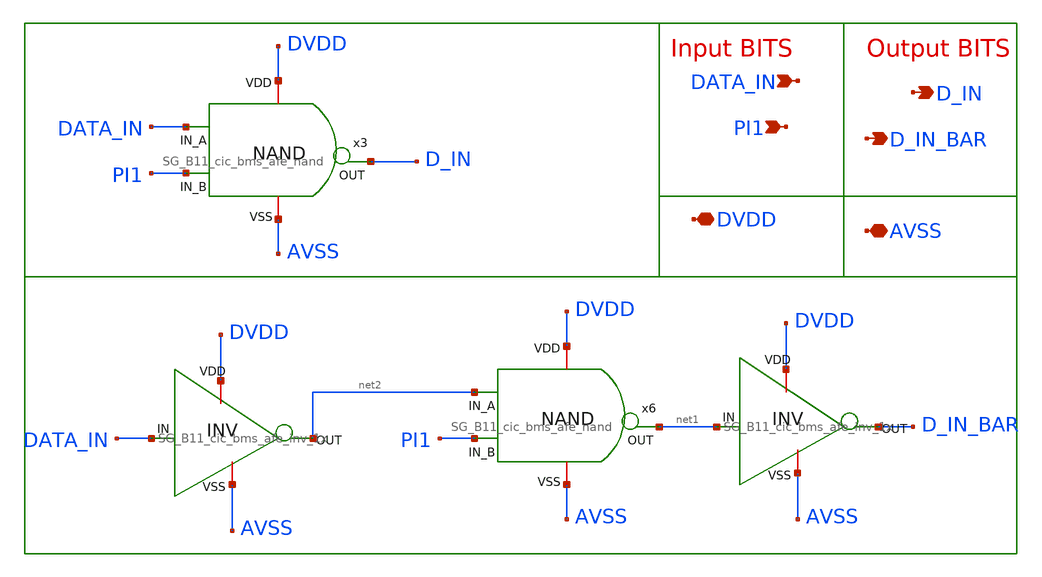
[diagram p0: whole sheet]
** sch_path: design/schematics/EIS/pkr_eis_control_logic.sch
**.subckt pkr_eis_control_logic DATA_IN PI1 DVDD AVSS D_IN D_IN_BAR
*.ipin DATA_IN
*.ipin PI1
*.iopin DVDD
*.iopin AVSS
*.opin D_IN
*.opin D_IN_BAR
x3 DVDD PI1 DATA_IN D_IN AVSS SG_B11_cic_bms_afe_nand
x5 DVDD D_IN_BAR net1 AVSS SG_B11_cic_bms_afe_inv_1x
x6 DVDD PI1 net2 net1 AVSS SG_B11_cic_bms_afe_nand
x4 DVDD net2 DATA_IN AVSS SG_B11_cic_bms_afe_inv_1x
**.ends

* expanding   symbol:  saakshath_designs/Non-overlapping _clk/SG_B11_cic_bms_afe_nand.sym # of
*+ pins=5
** sym_path: design/schematics/NOCG/SG_B11_cic_bms_afe_nand.sym
** sch_path: design/schematics/NOCG/SG_B11_cic_bms_afe_nand.sch
.subckt SG_B11_cic_bms_afe_nand VDD IN_B IN_A OUT VSS
*.iopin VDD
*.ipin IN_A
*.ipin IN_B
*.opin OUT
*.iopin VSS
XM1 OUT IN_A net1 VSS nfet_05v0 L=0.70u W=1.4u nf=1 ad='int((nf+1)/2) * W/nf * 0.18u' as='int((nf+2)/2) * W/nf * 0.18u'
+ pd='2*int((nf+1)/2) * (W/nf + 0.18u)' ps='2*int((nf+2)/2) * (W/nf + 0.18u)' nrd='0.18u / W' nrs='0.18u / W'
+ sa=0 sb=0 sd=0 m=1
XM2 net1 IN_B VSS VSS nfet_05v0 L=0.70u W=1.4u nf=1 ad='int((nf+1)/2) * W/nf * 0.18u' as='int((nf+2)/2) * W/nf * 0.18u'
+ pd='2*int((nf+1)/2) * (W/nf + 0.18u)' ps='2*int((nf+2)/2) * (W/nf + 0.18u)' nrd='0.18u / W' nrs='0.18u / W'
+ sa=0 sb=0 sd=0 m=1
XM3 OUT IN_B VDD VDD pfet_05v0 L=0.70u W=5.6u nf=1 ad='int((nf+1)/2) * W/nf * 0.18u' as='int((nf+2)/2) * W/nf * 0.18u'
+ pd='2*int((nf+1)/2) * (W/nf + 0.18u)' ps='2*int((nf+2)/2) * (W/nf + 0.18u)' nrd='0.18u / W' nrs='0.18u / W'
+ sa=0 sb=0 sd=0 m=1
XM4 OUT IN_A VDD VDD pfet_05v0 L=0.70u W=5.6u nf=1 ad='int((nf+1)/2) * W/nf * 0.18u' as='int((nf+2)/2) * W/nf * 0.18u'
+ pd='2*int((nf+1)/2) * (W/nf + 0.18u)' ps='2*int((nf+2)/2) * (W/nf + 0.18u)' nrd='0.18u / W' nrs='0.18u / W'
+ sa=0 sb=0 sd=0 m=1
.ends


* expanding   symbol:  saakshath_designs/Non-overlapping _clk/SG_B11_cic_bms_afe_inv_1x.sym # of
*+ pins=4
** sym_path: design/schematics/ADC/Non_Overlapping_clk_gen/SG_B11_cic_bms_afe_inv_1x.sym
** sch_path: design/schematics/ADC/Non_Overlapping_clk_gen/SG_B11_cic_bms_afe_inv_1x.sch
.subckt SG_B11_cic_bms_afe_inv_1x VDD OUT IN VSS
*.opin OUT
*.iopin VSS
*.iopin VDD
*.ipin IN
XM1 OUT IN VSS VSS nfet_05v0 L=0.70u W=1.4u nf=1 ad='int((nf+1)/2) * W/nf * 0.18u' as='int((nf+2)/2) * W/nf * 0.18u'
+ pd='2*int((nf+1)/2) * (W/nf + 0.18u)' ps='2*int((nf+2)/2) * (W/nf + 0.18u)' nrd='0.18u / W' nrs='0.18u / W'
+ sa=0 sb=0 sd=0 m=1
XM2 OUT IN VDD VDD pfet_05v0 L=0.70u W=5.6u nf=1 ad='int((nf+1)/2) * W/nf * 0.18u' as='int((nf+2)/2) * W/nf * 0.18u'
+ pd='2*int((nf+1)/2) * (W/nf + 0.18u)' ps='2*int((nf+2)/2) * (W/nf + 0.18u)' nrd='0.18u / W' nrs='0.18u / W'
+ sa=0 sb=0 sd=0 m=1
.ends

.end
